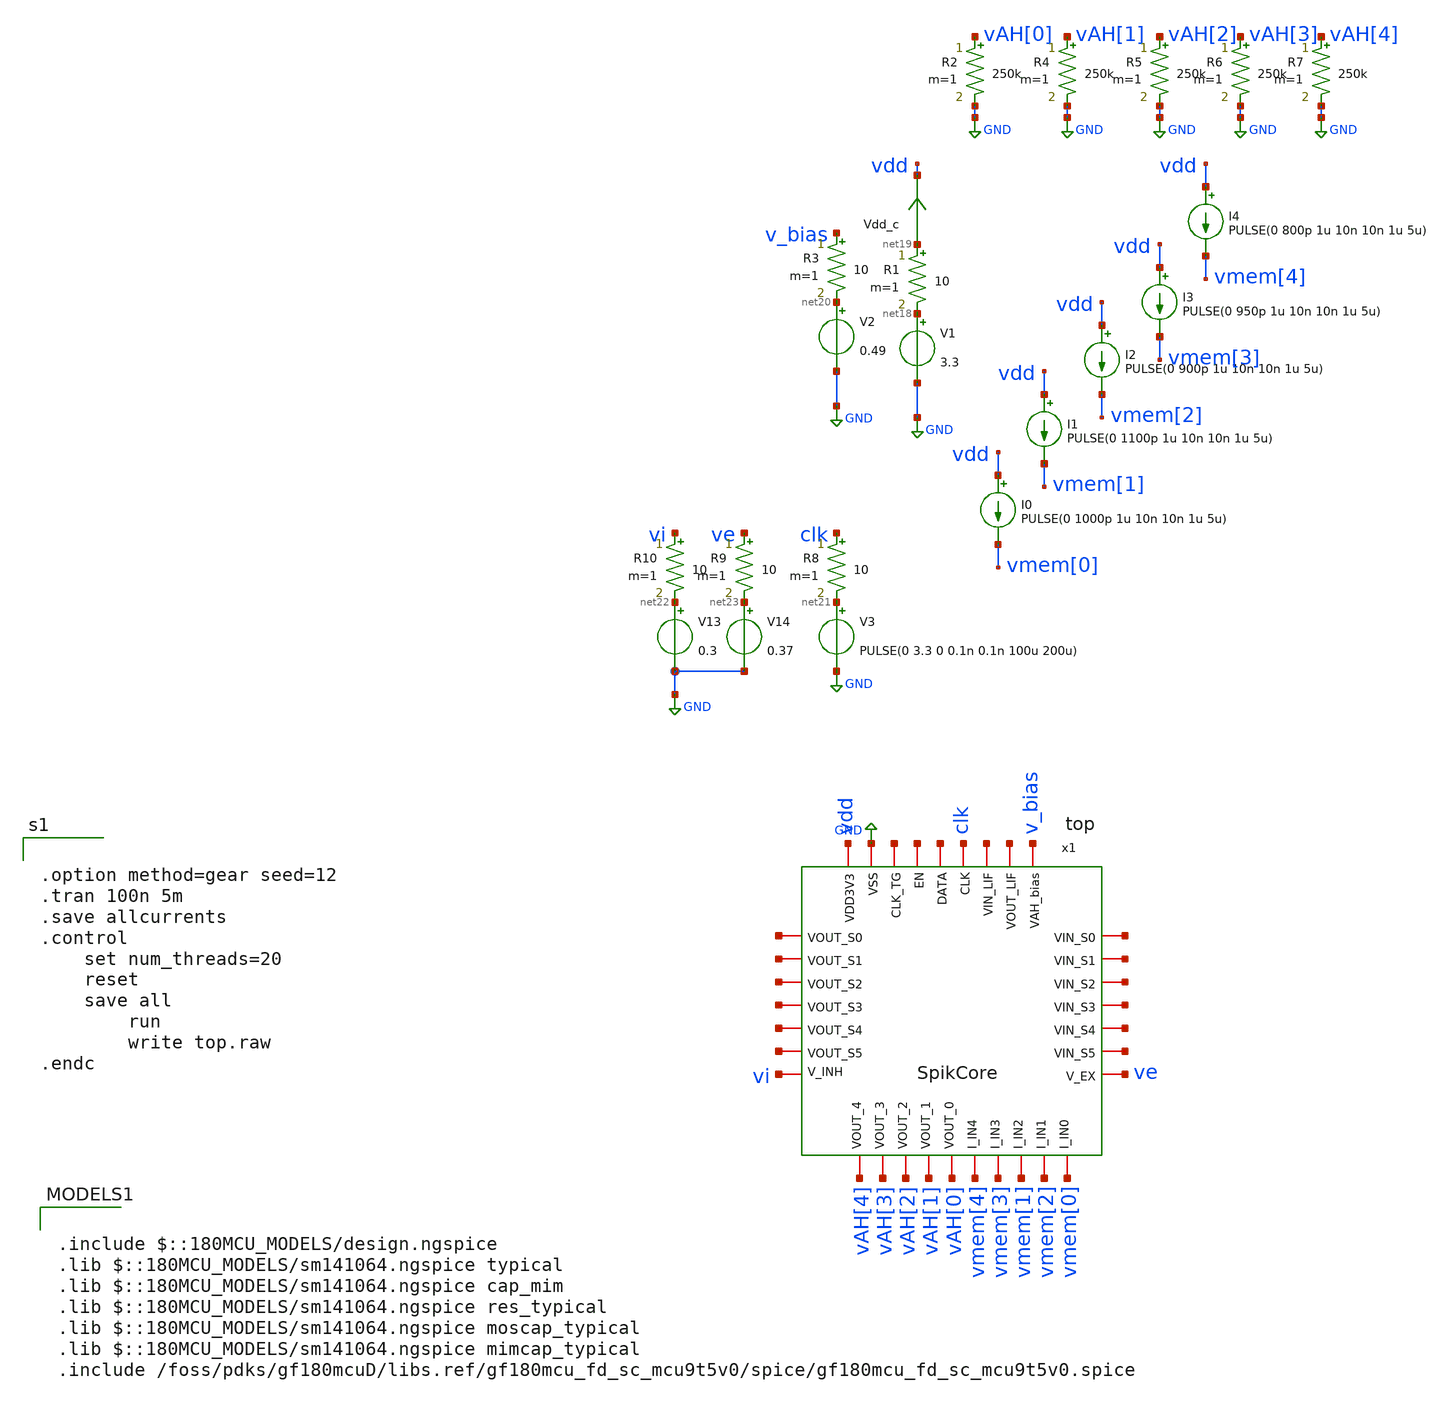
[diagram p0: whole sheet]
** sch_path: designs/libs/tb_top/top.sch
**.subckt top
x1 vdd GND net1 net2 net3 clk net4 net5 ve vi net6 net7 net8 net9 net10 net11 net12 net13 net14
+ net15 net16 net17 vmem[0] vAH[0] vmem[2] vAH[1] vmem[1] vAH[2] vmem[3] vAH[3] vmem[4] vAH[4] v_bias top
V1 net18 GND 3.3
Vdd_c net19 vdd 0
.save i(vdd_c)
I0 vdd vmem[0] PULSE(0 1000p 1u 10n 10n 1u 5u)
R1 net19 net18 10 m=1
R2 vAH[0] GND 250k m=1
V2 net20 GND 0.49
R3 v_bias net20 10 m=1
R4 vAH[1] GND 250k m=1
R5 vAH[2] GND 250k m=1
R6 vAH[3] GND 250k m=1
I1 vdd vmem[1] PULSE(0 1100p 1u 10n 10n 1u 5u)
I2 vdd vmem[2] PULSE(0 900p 1u 10n 10n 1u 5u)
I3 vdd vmem[3] PULSE(0 950p 1u 10n 10n 1u 5u)
R7 vAH[4] GND 250k m=1
I4 vdd vmem[4] PULSE(0 800p 1u 10n 10n 1u 5u)
V3 net21 GND PULSE(0 3.3 0 0.1n 0.1n 100u 200u)
R8 clk net21 10 m=1
V13 net22 GND 0.3
V14 net23 GND 0.37
R9 ve net23 10 m=1
R10 vi net22 10 m=1
**** begin user architecture code

.include $::180MCU_MODELS/design.ngspice
.lib $::180MCU_MODELS/sm141064.ngspice typical
.lib $::180MCU_MODELS/sm141064.ngspice cap_mim
.lib $::180MCU_MODELS/sm141064.ngspice res_typical
.lib $::180MCU_MODELS/sm141064.ngspice moscap_typical
.lib $::180MCU_MODELS/sm141064.ngspice mimcap_typical
.include /foss/pdks/gf180mcuD/libs.ref/gf180mcu_fd_sc_mcu9t5v0/spice/gf180mcu_fd_sc_mcu9t5v0.spice



.option method=gear seed=12
.tran 100n 5m
.save allcurrents
.control
	set num_threads=20
	reset
	save all
        run
        write top.raw
.endc


**** end user architecture code
**.ends
.GLOBAL GND
.end
